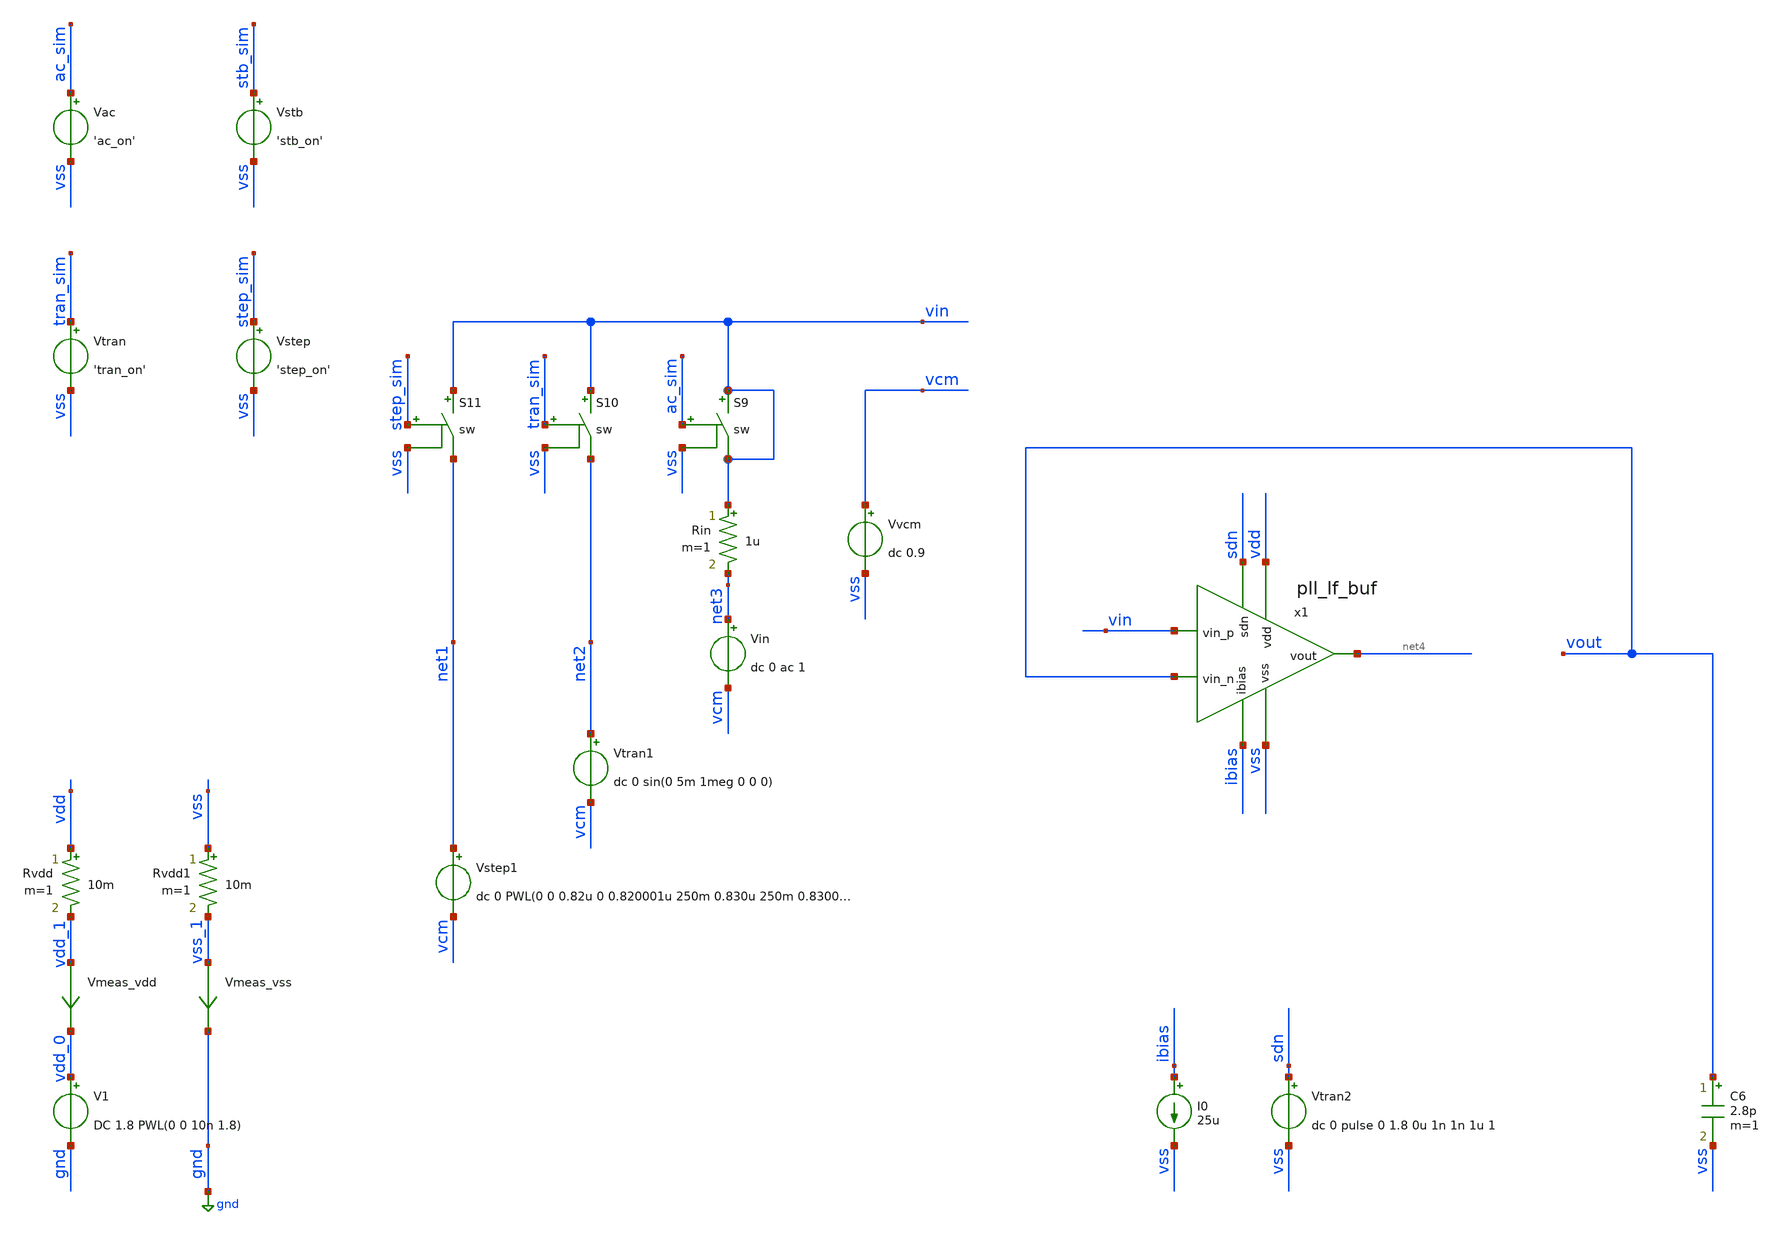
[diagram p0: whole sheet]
** sch_path: pll/pll_lf_buf/simulation/pll_lf_buf_tb.sch
**.subckt pll_lf_buf_tb
Vvcm vcm vss dc 0.9
C6 vout vss 2.8p m=1
Vtran tran_sim vss 'tran_on'
Vstep step_sim vss 'step_on'
Vstb stb_sim vss 'stb_on'
Vac ac_sim vss 'ac_on'
Vin net3 vcm dc 0 ac 1
S9 vin vin ac_sim vss sw
S10 vin net2 tran_sim vss sw
Vtran1 net2 vcm dc 0 sin(0 5m 1meg 0 0 0)
Vstep1 net1 vcm dc 0 PWL(0 0 0.82u 0 0.820001u 250m 0.830u 250m 0.830001u 0 0.86u 0 0.860001u -250m
+ 0.870u -250m 0.870001u 0)
S11 vin net1 step_sim vss sw
Rin vin net3 1u m=1
Vtran2 sdn vss dc 0 pulse 0 1.8 0u 1n 1n 1u 1
V1 vdd_0 gnd DC 1.8 PWL(0 0 10n 1.8)
Vmeas_vdd vdd_1 vdd_0 0
.save i(vmeas_vdd)
Vmeas_vss vss_1 gnd 0
.save i(vmeas_vss)
Rvdd vdd vdd_1 10m m=1
Rvdd1 vss vss_1 10m m=1
I0 ibias vss 25u
x1 vdd vin sdn vout net4 ibias vss pll_lf_buf
**** begin user architecture code


.param temp=27

.param ac_on=1
.param stb_on= 0
.param tran_on=0
.param step_on=0

.option savecurrents
.option rshunt = 1e12
*.option gmin = 1e-24
**.option method=Gear
**.option chgtol=1e-12


*.model switch1 aswitch(cntl_off=0.0 cntl_on=0.1 r_off=1e12 r_on=1.0 log=TRUE)
.model sw SW (ron=0.1 roff=1e12 vt=0.5 vh=0)

.control
* Main Amplifier
** Main Core OP params
save i(@m.x1.xm1.msky130_fd_pr__pfet_01v8[id])
save @m.x1.xm1.msky130_fd_pr__pfet_01v8[gm]
save v(@m.x1.xm1.msky130_fd_pr__pfet_01v8[vds])
save v(@m.x1.xm1.msky130_fd_pr__pfet_01v8[vgs])
save v(@m.x1.xm1.msky130_fd_pr__pfet_01v8[vth])
save v(@m.x1.xm1.msky130_fd_pr__pfet_01v8[vdsat])

save i(@m.x1.xm2.msky130_fd_pr__pfet_01v8[id])
save @m.x1.xm2.msky130_fd_pr__pfet_01v8[gm]
save v(@m.x1.xm2.msky130_fd_pr__pfet_01v8[vds])
save v(@m.x1.xm2.msky130_fd_pr__pfet_01v8[vgs])
save v(@m.x1.xm2.msky130_fd_pr__pfet_01v8[vth])
save v(@m.x1.xm2.msky130_fd_pr__pfet_01v8[vdsat])

save i(@m.x1.xm3.msky130_fd_pr__pfet_01v8[id])
save @m.x1.xm3.msky130_fd_pr__pfet_01v8[gm]
save v(@m.x1.xm3.msky130_fd_pr__pfet_01v8[vds])
save v(@m.x1.xm3.msky130_fd_pr__pfet_01v8[vgs])
save v(@m.x1.xm3.msky130_fd_pr__pfet_01v8[vth])
save v(@m.x1.xm3.msky130_fd_pr__pfet_01v8[vdsat])

save i(@m.x1.xm4.msky130_fd_pr__pfet_01v8[id])
save @m.x1.xm4.msky130_fd_pr__pfet_01v8[gm]
save v(@m.x1.xm4.msky130_fd_pr__pfet_01v8[vds])
save v(@m.x1.xm4.msky130_fd_pr__pfet_01v8[vgs])
save v(@m.x1.xm4.msky130_fd_pr__pfet_01v8[vth])
save v(@m.x1.xm4.msky130_fd_pr__pfet_01v8[vdsat])

save i(@m.x1.xm5.msky130_fd_pr__pfet_01v8[id])
save @m.x1.xm5.msky130_fd_pr__pfet_01v8[gm]
save v(@m.x1.xm5.msky130_fd_pr__pfet_01v8[vds])
save v(@m.x1.xm5.msky130_fd_pr__pfet_01v8[vgs])
save v(@m.x1.xm5.msky130_fd_pr__pfet_01v8[vth])
save v(@m.x1.xm5.msky130_fd_pr__pfet_01v8[vdsat])

save i(@m.x1.xm6.msky130_fd_pr__pfet_01v8[id])
save @m.x1.xm6.msky130_fd_pr__pfet_01v8[gm]
save v(@m.x1.xm6.msky130_fd_pr__pfet_01v8[vds])
save v(@m.x1.xm6.msky130_fd_pr__pfet_01v8[vgs])
save v(@m.x1.xm6.msky130_fd_pr__pfet_01v8[vth])
save v(@m.x1.xm6.msky130_fd_pr__pfet_01v8[vdsat])

save i(@m.x1.xm7.msky130_fd_pr__nfet_01v8[id])
save @m.x1.xm7.msky130_fd_pr__nfet_01v8[gm]
save v(@m.x1.xm7.msky130_fd_pr__nfet_01v8[vds])
save v(@m.x1.xm7.msky130_fd_pr__nfet_01v8[vgs])
save v(@m.x1.xm7.msky130_fd_pr__nfet_01v8[vth])
save v(@m.x1.xm7.msky130_fd_pr__nfet_01v8[vdsat])

save i(@m.x1.xm8.msky130_fd_pr__nfet_01v8[id])
save @m.x1.xm8.msky130_fd_pr__nfet_01v8[gm]
save v(@m.x1.xm8.msky130_fd_pr__nfet_01v8[vds])
save v(@m.x1.xm8.msky130_fd_pr__nfet_01v8[vgs])
save v(@m.x1.xm8.msky130_fd_pr__nfet_01v8[vth])
save v(@m.x1.xm8.msky130_fd_pr__nfet_01v8[vdsat])

save i(@m.x1.xm9.msky130_fd_pr__nfet_01v8[id])
save @m.x1.xm9.msky130_fd_pr__nfet_01v8[gm]
save v(@m.x1.xm9.msky130_fd_pr__nfet_01v8[vds])
save v(@m.x1.xm9.msky130_fd_pr__nfet_01v8[vgs])
save v(@m.x1.xm9.msky130_fd_pr__nfet_01v8[vth])
save v(@m.x1.xm9.msky130_fd_pr__nfet_01v8[vdsat])

save i(@m.x1.xm10.msky130_fd_pr__nfet_01v8[id])
save @m.x1.xm10.msky130_fd_pr__nfet_01v8[gm]
save v(@m.x1.xm10.msky130_fd_pr__nfet_01v8[vds])
save v(@m.x1.xm10.msky130_fd_pr__nfet_01v8[vgs])
save v(@m.x1.xm10.msky130_fd_pr__nfet_01v8[vth])
save v(@m.x1.xm10.msky130_fd_pr__nfet_01v8[vdsat])

save i(@m.x1.xm11.msky130_fd_pr__pfet_01v8[id])
save @m.x1.xm11.msky130_fd_pr__pfet_01v8[gm]
save v(@m.x1.xm11.msky130_fd_pr__pfet_01v8[vds])
save v(@m.x1.xm11.msky130_fd_pr__pfet_01v8[vgs])
save v(@m.x1.xm11.msky130_fd_pr__pfet_01v8[vth])
save v(@m.x1.xm11.msky130_fd_pr__pfet_01v8[vdsat])


** CMFB OP param
save i(@m.x1.xm28.msky130_fd_pr__pfet_01v8[id])
save @m.x1.xm28.msky130_fd_pr__pfet_01v8[gm]
save v(@m.x1.xm28.msky130_fd_pr__pfet_01v8[vds])
save v(@m.x1.xm28.msky130_fd_pr__pfet_01v8[vgs])
save v(@m.x1.xm28.msky130_fd_pr__pfet_01v8[vth])
save v(@m.x1.xm28.msky130_fd_pr__pfet_01v8[vdsat])

save i(@m.x1.xm29.msky130_fd_pr__pfet_01v8_lvt[id])
save @m.x1.xm29.msky130_fd_pr__pfet_01v8_lvt[gm]
save v(@m.x1.xm29.msky130_fd_pr__pfet_01v8_lvt[vds])
save v(@m.x1.xm29.msky130_fd_pr__pfet_01v8_lvt[vgs])
save v(@m.x1.xm29.msky130_fd_pr__pfet_01v8_lvt[vth])
save v(@m.x1.xm29.msky130_fd_pr__pfet_01v8_lvt[vdsat])

save i(@m.x1.xm30.msky130_fd_pr__pfet_01v8_lvt[id])
save @m.x1.xm30.msky130_fd_pr__pfet_01v8_lvt[gm]
save v(@m.x1.xm30.msky130_fd_pr__pfet_01v8_lvt[vds])
save v(@m.x1.xm30.msky130_fd_pr__pfet_01v8_lvt[vgs])
save v(@m.x1.xm30.msky130_fd_pr__pfet_01v8_lvt[vth])
save v(@m.x1.xm30.msky130_fd_pr__pfet_01v8_lvt[vdsat])

save i(@m.x1.xm31.msky130_fd_pr__pfet_01v8[id])
save @m.x1.xm31.msky130_fd_pr__pfet_01v8[gm]
save v(@m.x1.xm31.msky130_fd_pr__pfet_01v8[vds])
save v(@m.x1.xm31.msky130_fd_pr__pfet_01v8[vgs])
save v(@m.x1.xm31.msky130_fd_pr__pfet_01v8[vth])
save v(@m.x1.xm31.msky130_fd_pr__pfet_01v8[vdsat])

save i(@m.x1.xm32.msky130_fd_pr__pfet_01v8_lvt[id])
save @m.x1.xm32.msky130_fd_pr__pfet_01v8_lvt[gm]
save v(@m.x1.xm32.msky130_fd_pr__pfet_01v8_lvt[vds])
save v(@m.x1.xm32.msky130_fd_pr__pfet_01v8_lvt[vgs])
save v(@m.x1.xm32.msky130_fd_pr__pfet_01v8_lvt[vth])
save v(@m.x1.xm32.msky130_fd_pr__pfet_01v8_lvt[vdsat])

save i(@m.x1.xm33.msky130_fd_pr__pfet_01v8_lvt[id])
save @m.x1.xm33.msky130_fd_pr__pfet_01v8_lvt[gm]
save v(@m.x1.xm33.msky130_fd_pr__pfet_01v8_lvt[vds])
save v(@m.x1.xm33.msky130_fd_pr__pfet_01v8_lvt[vgs])
save v(@m.x1.xm33.msky130_fd_pr__pfet_01v8_lvt[vth])
save v(@m.x1.xm33.msky130_fd_pr__pfet_01v8_lvt[vdsat])

save i(@m.x1.xm34.msky130_fd_pr__nfet_01v8[id])
save @m.x1.xm34.msky130_fd_pr__nfet_01v8[gm]
save v(@m.x1.xm34.msky130_fd_pr__nfet_01v8[vds])
save v(@m.x1.xm34.msky130_fd_pr__nfet_01v8[vgs])
save v(@m.x1.xm34.msky130_fd_pr__nfet_01v8[vth])
save v(@m.x1.xm34.msky130_fd_pr__nfet_01v8[vdsat])

save i(@m.x1.xm35.msky130_fd_pr__nfet_01v8[id])
save @m.x1.xm35.msky130_fd_pr__nfet_01v8[gm]
save v(@m.x1.xm35.msky130_fd_pr__nfet_01v8[vds])
save v(@m.x1.xm35.msky130_fd_pr__nfet_01v8[vgs])
save v(@m.x1.xm35.msky130_fd_pr__nfet_01v8[vth])
save v(@m.x1.xm35.msky130_fd_pr__nfet_01v8[vdsat])

* Gain Booster Pside
** Main core OP parameters
save i(@m.x1.xgbp.xm1.msky130_fd_pr__nfet_01v8[id])
save @m.x1.xgbp.xm1.msky130_fd_pr__nfet_01v8[gm]
save v(@m.x1.xgbp.xm1.msky130_fd_pr__nfet_01v8[vds])
save v(@m.x1.xgbp.xm1.msky130_fd_pr__nfet_01v8[vgs])
save v(@m.x1.xgbp.xm1.msky130_fd_pr__nfet_01v8[vth])
save v(@m.x1.xgbp.xm1.msky130_fd_pr__nfet_01v8[vdsat])

save i(@m.x1.xgbp.xm2.msky130_fd_pr__nfet_01v8[id])
save @m.x1.xgbp.xm2.msky130_fd_pr__nfet_01v8[gm]
save v(@m.x1.xgbp.xm2.msky130_fd_pr__nfet_01v8[vds])
save v(@m.x1.xgbp.xm2.msky130_fd_pr__nfet_01v8[vgs])
save v(@m.x1.xgbp.xm2.msky130_fd_pr__nfet_01v8[vth])
save v(@m.x1.xgbp.xm2.msky130_fd_pr__nfet_01v8[vdsat])

save i(@m.x1.xgbp.xm3.msky130_fd_pr__nfet_01v8[id])
save @m.x1.xgbp.xm3.msky130_fd_pr__nfet_01v8[gm]
save v(@m.x1.xgbp.xm3.msky130_fd_pr__nfet_01v8[vds])
save v(@m.x1.xgbp.xm3.msky130_fd_pr__nfet_01v8[vgs])
save v(@m.x1.xgbp.xm3.msky130_fd_pr__nfet_01v8[vth])
save v(@m.x1.xgbp.xm3.msky130_fd_pr__nfet_01v8[vdsat])

save i(@m.x1.xgbp.xm4.msky130_fd_pr__pfet_01v8[id])
save @m.x1.xgbp.xm4.msky130_fd_pr__pfet_01v8[gm]
save v(@m.x1.xgbp.xm4.msky130_fd_pr__pfet_01v8[vds])
save v(@m.x1.xgbp.xm4.msky130_fd_pr__pfet_01v8[vgs])
save v(@m.x1.xgbp.xm4.msky130_fd_pr__pfet_01v8[vth])
save v(@m.x1.xgbp.xm4.msky130_fd_pr__pfet_01v8[vdsat])

save i(@m.x1.xgbp.xm5.msky130_fd_pr__pfet_01v8[id])
save @m.x1.xgbp.xm5.msky130_fd_pr__pfet_01v8[gm]
save v(@m.x1.xgbp.xm5.msky130_fd_pr__pfet_01v8[vds])
save v(@m.x1.xgbp.xm5.msky130_fd_pr__pfet_01v8[vgs])
save v(@m.x1.xgbp.xm5.msky130_fd_pr__pfet_01v8[vth])
save v(@m.x1.xgbp.xm5.msky130_fd_pr__pfet_01v8[vdsat])

save i(@m.x1.xgbp.xm6.msky130_fd_pr__pfet_01v8[id])
save @m.x1.xgbp.xm6.msky130_fd_pr__pfet_01v8[gm]
save v(@m.x1.xgbp.xm6.msky130_fd_pr__pfet_01v8[vds])
save v(@m.x1.xgbp.xm6.msky130_fd_pr__pfet_01v8[vgs])
save v(@m.x1.xgbp.xm6.msky130_fd_pr__pfet_01v8[vth])
save v(@m.x1.xgbp.xm6.msky130_fd_pr__pfet_01v8[vdsat])

save i(@m.x1.xgbp.xm7.msky130_fd_pr__pfet_01v8[id])
save @m.x1.xgbp.xm7.msky130_fd_pr__pfet_01v8[gm]
save v(@m.x1.xgbp.xm7.msky130_fd_pr__pfet_01v8[vds])
save v(@m.x1.xgbp.xm7.msky130_fd_pr__pfet_01v8[vgs])
save v(@m.x1.xgbp.xm7.msky130_fd_pr__pfet_01v8[vth])
save v(@m.x1.xgbp.xm7.msky130_fd_pr__pfet_01v8[vdsat])

save i(@m.x1.xgbp.xm8.msky130_fd_pr__nfet_01v8[id])
save @m.x1.xgbp.xm8.msky130_fd_pr__nfet_01v8[gm]
save v(@m.x1.xgbp.xm8.msky130_fd_pr__nfet_01v8[vds])
save v(@m.x1.xgbp.xm8.msky130_fd_pr__nfet_01v8[vgs])
save v(@m.x1.xgbp.xm8.msky130_fd_pr__nfet_01v8[vth])
save v(@m.x1.xgbp.xm8.msky130_fd_pr__nfet_01v8[vdsat])

save i(@m.x1.xgbp.xm9.msky130_fd_pr__nfet_01v8[id])
save @m.x1.xgbp.xm9.msky130_fd_pr__nfet_01v8[gm]
save v(@m.x1.xgbp.xm9.msky130_fd_pr__nfet_01v8[vds])
save v(@m.x1.xgbp.xm9.msky130_fd_pr__nfet_01v8[vgs])
save v(@m.x1.xgbp.xm9.msky130_fd_pr__nfet_01v8[vth])
save v(@m.x1.xgbp.xm9.msky130_fd_pr__nfet_01v8[vdsat])

save i(@m.x1.xgbp.xm10.msky130_fd_pr__nfet_01v8[id])
save @m.x1.xgbp.xm10.msky130_fd_pr__nfet_01v8[gm]
save v(@m.x1.xgbp.xm10.msky130_fd_pr__nfet_01v8[vds])
save v(@m.x1.xgbp.xm10.msky130_fd_pr__nfet_01v8[vgs])
save v(@m.x1.xgbp.xm10.msky130_fd_pr__nfet_01v8[vth])
save v(@m.x1.xgbp.xm10.msky130_fd_pr__nfet_01v8[vdsat])

save i(@m.x1.xgbp.xm11.msky130_fd_pr__nfet_01v8[id])
save @m.x1.xgbp.xm11.msky130_fd_pr__nfet_01v8[gm]
save v(@m.x1.xgbp.xm11.msky130_fd_pr__nfet_01v8[vds])
save v(@m.x1.xgbp.xm11.msky130_fd_pr__nfet_01v8[vgs])
save v(@m.x1.xgbp.xm11.msky130_fd_pr__nfet_01v8[vth])
save v(@m.x1.xgbp.xm11.msky130_fd_pr__nfet_01v8[vdsat])


** CMFB OP param
save i(@m.x1.xgbp.xm28.msky130_fd_pr__pfet_01v8[id])
save @m.x1.xgbp.xm28.msky130_fd_pr__pfet_01v8[gm]
save v(@m.x1.xgbp.xm28.msky130_fd_pr__pfet_01v8[vds])
save v(@m.x1.xgbp.xm28.msky130_fd_pr__pfet_01v8[vgs])
save v(@m.x1.xgbp.xm28.msky130_fd_pr__pfet_01v8[vth])
save v(@m.x1.xgbp.xm28.msky130_fd_pr__pfet_01v8[vdsat])

save i(@m.x1.xgbp.xm29.msky130_fd_pr__pfet_01v8_lvt[id])
save @m.x1.xgbp.xm29.msky130_fd_pr__pfet_01v8_lvt[gm]
save v(@m.x1.xgbp.xm29.msky130_fd_pr__pfet_01v8_lvt[vds])
save v(@m.x1.xgbp.xm29.msky130_fd_pr__pfet_01v8_lvt[vgs])
save v(@m.x1.xgbp.xm29.msky130_fd_pr__pfet_01v8_lvt[vth])
save v(@m.x1.xgbp.xm29.msky130_fd_pr__pfet_01v8_lvt[vdsat])

save i(@m.x1.xgbp.xm30.msky130_fd_pr__pfet_01v8_lvt[id])
save @m.x1.xgbp.xm30.msky130_fd_pr__pfet_01v8_lvt[gm]
save v(@m.x1.xgbp.xm30.msky130_fd_pr__pfet_01v8_lvt[vds])
save v(@m.x1.xgbp.xm30.msky130_fd_pr__pfet_01v8_lvt[vgs])
save v(@m.x1.xgbp.xm30.msky130_fd_pr__pfet_01v8_lvt[vth])
save v(@m.x1.xgbp.xm30.msky130_fd_pr__pfet_01v8_lvt[vdsat])

save i(@m.x1.xgbp.xm31.msky130_fd_pr__pfet_01v8[id])
save @m.x1.xgbp.xm31.msky130_fd_pr__pfet_01v8[gm]
save v(@m.x1.xgbp.xm31.msky130_fd_pr__pfet_01v8[vds])
save v(@m.x1.xgbp.xm31.msky130_fd_pr__pfet_01v8[vgs])
save v(@m.x1.xgbp.xm31.msky130_fd_pr__pfet_01v8[vth])
save v(@m.x1.xgbp.xm31.msky130_fd_pr__pfet_01v8[vdsat])

save i(@m.x1.xgbp.xm32.msky130_fd_pr__pfet_01v8_lvt[id])
save @m.x1.xgbp.xm32.msky130_fd_pr__pfet_01v8_lvt[gm]
save v(@m.x1.xgbp.xm32.msky130_fd_pr__pfet_01v8_lvt[vds])
save v(@m.x1.xgbp.xm32.msky130_fd_pr__pfet_01v8_lvt[vgs])
save v(@m.x1.xgbp.xm32.msky130_fd_pr__pfet_01v8_lvt[vth])
save v(@m.x1.xgbp.xm32.msky130_fd_pr__pfet_01v8_lvt[vdsat])

save i(@m.x1.xgbp.xm33.msky130_fd_pr__pfet_01v8_lvt[id])
save @m.x1.xgbp.xm33.msky130_fd_pr__pfet_01v8_lvt[gm]
save v(@m.x1.xgbp.xm33.msky130_fd_pr__pfet_01v8_lvt[vds])
save v(@m.x1.xgbp.xm33.msky130_fd_pr__pfet_01v8_lvt[vgs])
save v(@m.x1.xgbp.xm33.msky130_fd_pr__pfet_01v8_lvt[vth])
save v(@m.x1.xgbp.xm33.msky130_fd_pr__pfet_01v8_lvt[vdsat])

save i(@m.x1.xgbp.xm34.msky130_fd_pr__nfet_01v8[id])
save @m.x1.xgbp.xm34.msky130_fd_pr__nfet_01v8[gm]
save v(@m.x1.xgbp.xm34.msky130_fd_pr__nfet_01v8[vds])
save v(@m.x1.xgbp.xm34.msky130_fd_pr__nfet_01v8[vgs])
save v(@m.x1.xgbp.xm34.msky130_fd_pr__nfet_01v8[vth])
save v(@m.x1.xgbp.xm34.msky130_fd_pr__nfet_01v8[vdsat])

save i(@m.x1.xgbp.xm35.msky130_fd_pr__nfet_01v8[id])
save @m.x1.xgbp.xm35.msky130_fd_pr__nfet_01v8[gm]
save v(@m.x1.xgbp.xm35.msky130_fd_pr__nfet_01v8[vds])
save v(@m.x1.xgbp.xm35.msky130_fd_pr__nfet_01v8[vgs])
save v(@m.x1.xgbp.xm35.msky130_fd_pr__nfet_01v8[vth])
save v(@m.x1.xgbp.xm35.msky130_fd_pr__nfet_01v8[vdsat])


* #################################################################
* #
* #                         OPERATING POINT
* #
* #################################################################
save all
save v(vin)
save v(vout)

op
set filetype=binary
write pll_lf_buf_tb.raw all


* #################################################################
* #
* #                          AC SIMULATION
* #
* #################################################################
alterparam ac_on=1
alterparam stb_on=0
alterparam tran_on=0
alterparam step_on=0
reset
save all
save v(vin)
save v(vout)

ac dec 100 1 1T
set filetype=ascii
write  pll_lf_buf_tb_ac.raw all

plot dB(v(vout)/v(vin))


* #################################################################
* #
* #                     STABILITY SIMULATION
* #
* #################################################################
alterparam ac_on=1
alterparam stb_on=0
alterparam tran_on=0
alterparam step_on=0
reset
save all
save v(vin)
save v(vout)

*set mag_ac = @Vin[acmag]
alter @Vin[acmag]=0
*set imp_ac = @Rin[r]
alter @Rin[r]=1e12

alter @v.xstbprb.Vprobe1[acmag]=1
alter @i.xstbprb.Iprobe1[acmag]=0
ac dec 100 1 1T
set filetype=ascii
write pll_lf_buf_tb_ol_0.raw all

alter @v.xstbprb.Vprobe1[acmag]=0
alter @i.xstbprb.Iprobe1[acmag]=1
ac dec 100 1 1T
set filetype=ascii
write pll_lf_buf_tb_ol_1.raw all

alter @v.xstbprb.Vprobe1[acmag]=0
alter @i.xstbprb.Iprobe1[acmag]=0

*alter @Vin[acmag]=mag_ac
*alter @Rin[r]=imp_ac
alter @Vin[acmag]=1
alter @Rin[r]=1u


* EXTRACT REQUIRED DATA
let ip11 = ac2.i(v.xstbprb.Vprobe1)
let ip12 = ac2.i(v.xstbprb.Vprobe2)
let ip21 = ac3.i(v.xstbprb.Vprobe1)
let ip22 = ac3.i(v.xstbprb.Vprobe2)
let vprb1 = ac2.xstbprb.probe_p
let vprb2 = ac3.xstbprb.probe_p
*let vprb1 = ac2.xstbprb.probe_p-ac2.xstbprb.probe_n
*let vprb2 = ac3.xstbprb.probe_p-ac3.xstbprb.probe_n


* MIDDLEBROOK
let loopgain_middlebrook = 1/(vprb1+ip22)-1
let phase_middlebrook = 180/PI*vp(loopgain_middlebrook)

* TIAN
let loopgain_tian = 1/(1/(2*(ip11*vprb2-vprb1*ip21)+vprb1+ip21)-1)
let phase_tian = 180/PI*vp(loopgain_tian)

* CALCULATE & PLOT
plot vdb(loopgain_tian)
plot phase_tian

plot vdb(loopgain_middlebrook)
plot phase_middlebrook

plot vdb(loopgain_middlebrook) vdb(loopgain_tian)
plot phase_middlebrook phase_tian

* MEASUREMENT
echo --
echo --
let pm_deg=0
let pm_freq=0
meas ac pm_deg find phase_tian when vdb(loopgain_tian)=0
meas ac pm_freq find frequency when vdb(loopgain_tian)=0

let gm_db=0
let gm_freq=0
meas ac gm_db find vdb(loopgain_tian) when vp(loopgain_tian)=0
meas ac gm_freq find frequency when vp(loopgain_tian)=0

*meas ac 3db_f when phase_tian=135
*meas ac 0db_f when vdb(loopgain_tian)=0
*meas ac dc_gain find vdb(loopgain_tian) at=0.01
*meas ac m6dB when vdB(loopgain_tian)=-6
echo --
echo --

* SAVE DATA
set filetype=ascii
write  pll_lf_buf_tb_ol.raw loopgain_middlebrook loopgain_tian pm_deg pm_freq gm_db gm_freq

* #################################################################
* #
* #                       NOISE SIMULATION
* #
* #################################################################
alterparam ac_on=1
alterparam stb_on=0
alterparam tran_on=0
alterparam step_on=0
reset
save all
save v(vin)
save v(vout)

set sqrnoise
noise v(vout) vin dec 100 1 1T
set filetype=ascii
write  pll_lf_buf_se_tb_noise.raw all noise3.inoise_spectrum noise3.onoise_spectrum

plot noise3.inoise_spectrum noise3.onoise_spectrum
print inoise_total
print onoise_total

* #################################################################
* #
* #                 TRANSIENT SINE WAVE REGIME
* #
* #################################################################
alterparam ac_on=0
alterparam stb_on=0
alterparam tran_on=1
alterparam step_on=0
reset
save all
save v(vin)
save v(vout)

set imp_ac = @Rin[r]
alter @Rin[r]=1e12

tran 0.1n 10u uic
set filetype=ascii
write pll_lf_buf_tb_tran.raw all

alter @Rin[r]=imp_ac

plot v(vin) v(vout)


* #################################################################
* #
* #                   TRANSIENT STEP RESPONSE
* #
* #################################################################
*alterparam ac_on = 0
*alterparam stb_on = 0
*alterparam tran_on = 0
*alterparam step_on = 1
*reset
*save all
*save v(vin)
*save v(vout)
*
*set imp_ac = @Rin[r]
*alter @Rin[r]=1e12
*
*tran 0.1n 0.9u 0.8u
*set filetype=ascii
*write pll_lf_buf_tb_step.raw all
*
*alter @Rin[r]=imp_ac
*
*plot v(vin) v(vout)

.endc



.options wnflag=1
.include $::SKYWATER_MODELS/cells/nfet_01v8/sky130_fd_pr__nfet_01v8__tt.corner.spice
.include $::SKYWATER_MODELS/cells/nfet_01v8_lvt/sky130_fd_pr__nfet_01v8_lvt__tt.corner.spice
.include $::SKYWATER_MODELS/cells/pfet_01v8/sky130_fd_pr__pfet_01v8__tt.corner.spice
.include $::SKYWATER_MODELS/cells/nfet_03v3_nvt/sky130_fd_pr__nfet_03v3_nvt__tt.corner.spice
.include $::SKYWATER_MODELS/cells/nfet_05v0_nvt/sky130_fd_pr__nfet_05v0_nvt__tt.corner.spice
.include $::SKYWATER_MODELS/cells/esd_nfet_01v8/sky130_fd_pr__esd_nfet_01v8__tt.corner.spice
.include $::SKYWATER_MODELS/cells/pfet_01v8_lvt/sky130_fd_pr__pfet_01v8_lvt__tt.corner.spice
.include $::SKYWATER_MODELS/cells/pfet_01v8_hvt/sky130_fd_pr__pfet_01v8_hvt__tt.corner.spice
.include $::SKYWATER_MODELS/cells/esd_pfet_g5v0d10v5/sky130_fd_pr__esd_pfet_g5v0d10v5__tt.corner.spice
.include $::SKYWATER_MODELS/cells/pfet_g5v0d10v5/sky130_fd_pr__pfet_g5v0d10v5__tt.corner.spice
.include $::SKYWATER_MODELS/cells/pfet_g5v0d16v0/sky130_fd_pr__pfet_g5v0d16v0__tt.corner.spice
.include $::SKYWATER_MODELS/cells/nfet_g5v0d10v5/sky130_fd_pr__nfet_g5v0d10v5__tt.corner.spice
.include $::SKYWATER_MODELS/cells/nfet_g5v0d16v0/sky130_fd_pr__nfet_g5v0d16v0__tt_discrete.corner.spice
.include $::SKYWATER_MODELS/cells/esd_nfet_g5v0d10v5/sky130_fd_pr__esd_nfet_g5v0d10v5__tt.corner.spice
.include $::SKYWATER_MODELS/models/corners/tt/nonfet.spice
* Mismatch parameters
.include $::SKYWATER_MODELS/cells/nfet_01v8/sky130_fd_pr__nfet_01v8__mismatch.corner.spice
.include $::SKYWATER_MODELS/cells/pfet_01v8/sky130_fd_pr__pfet_01v8__mismatch.corner.spice
.include $::SKYWATER_MODELS/cells/nfet_01v8_lvt/sky130_fd_pr__nfet_01v8_lvt__mismatch.corner.spice
.include $::SKYWATER_MODELS/cells/pfet_01v8_lvt/sky130_fd_pr__pfet_01v8_lvt__mismatch.corner.spice
.include $::SKYWATER_MODELS/cells/pfet_01v8_hvt/sky130_fd_pr__pfet_01v8_hvt__mismatch.corner.spice
.include $::SKYWATER_MODELS/cells/nfet_g5v0d10v5/sky130_fd_pr__nfet_g5v0d10v5__mismatch.corner.spice
.include $::SKYWATER_MODELS/cells/pfet_g5v0d10v5/sky130_fd_pr__pfet_g5v0d10v5__mismatch.corner.spice
.include $::SKYWATER_MODELS/cells/nfet_05v0_nvt/sky130_fd_pr__nfet_05v0_nvt__mismatch.corner.spice
.include $::SKYWATER_MODELS/cells/nfet_03v3_nvt/sky130_fd_pr__nfet_03v3_nvt__mismatch.corner.spice
* Resistor$::SKYWATER_MODELS/Capacitor
.include $::SKYWATER_MODELS/models/r+c/res_typical__cap_typical.spice
.include $::SKYWATER_MODELS/models/r+c/res_typical__cap_typical__lin.spice
* Special cells
.include $::SKYWATER_MODELS/models/corners/tt/specialized_cells.spice
* All models
.include $::SKYWATER_MODELS/models/all.spice
* Corner
.include $::SKYWATER_MODELS/models/corners/tt/rf.spice

**** end user architecture code
**.ends

* expanding   symbol:  test_jens/pll/pll_lf_buf/pll_lf_buf.sym # of pins=7
** sym_path: pll/pll_lf_buf/xschem/pll_lf_buf.sym
** sch_path: pll/pll_lf_buf/xschem/pll_lf_buf.sch
.subckt pll_lf_buf vdd vin_p sdn vin_n vout ibias vss
*.iopin vss
*.iopin vdd
*.ipin vin_p
*.ipin vin_n
*.iopin ibias
*.opin vout
*.ipin sdn
XM1 net4 vin_p net1 vdd sky130_fd_pr__pfet_01v8 L=0.15 W=16 nf=2 ad='int((nf+1)/2) * W/nf * 0.29' as='int((nf+2)/2) * W/nf * 0.29'
+ pd='2*int((nf+1)/2) * (W/nf + 0.29)' ps='2*int((nf+2)/2) * (W/nf + 0.29)' nrd='0.29 / W' nrs='0.29 / W'
+ sa=0 sb=0 sd=0 mult=8 m=8
XM2 net5 vin_n net1 vdd sky130_fd_pr__pfet_01v8 L=0.15 W=16 nf=2 ad='int((nf+1)/2) * W/nf * 0.29' as='int((nf+2)/2) * W/nf * 0.29'
+ pd='2*int((nf+1)/2) * (W/nf + 0.29)' ps='2*int((nf+2)/2) * (W/nf + 0.29)' nrd='0.29 / W' nrs='0.29 / W'
+ sa=0 sb=0 sd=0 mult=8 m=8
XM3 vbn vbp_casc net2 vdd sky130_fd_pr__pfet_01v8 L=0.3 W=16 nf=2 ad='int((nf+1)/2) * W/nf * 0.29' as='int((nf+2)/2) * W/nf * 0.29'
+ pd='2*int((nf+1)/2) * (W/nf + 0.29)' ps='2*int((nf+2)/2) * (W/nf + 0.29)' nrd='0.29 / W' nrs='0.29 / W'
+ sa=0 sb=0 sd=0 mult=8 m=8
XM4 vout vbp_casc net3 vdd sky130_fd_pr__pfet_01v8 L=0.3 W=16 nf=2 ad='int((nf+1)/2) * W/nf * 0.29' as='int((nf+2)/2) * W/nf * 0.29'
+ pd='2*int((nf+1)/2) * (W/nf + 0.29)' ps='2*int((nf+2)/2) * (W/nf + 0.29)' nrd='0.29 / W' nrs='0.29 / W'
+ sa=0 sb=0 sd=0 mult=8 m=8
XM5 net2 vbp vdd vdd sky130_fd_pr__pfet_01v8 L=0.3 W=16 nf=2 ad='int((nf+1)/2) * W/nf * 0.29' as='int((nf+2)/2) * W/nf * 0.29'
+ pd='2*int((nf+1)/2) * (W/nf + 0.29)' ps='2*int((nf+2)/2) * (W/nf + 0.29)' nrd='0.29 / W' nrs='0.29 / W'
+ sa=0 sb=0 sd=0 mult=8 m=8
XM6 net3 vbp vdd vdd sky130_fd_pr__pfet_01v8 L=0.3 W=16 nf=2 ad='int((nf+1)/2) * W/nf * 0.29' as='int((nf+2)/2) * W/nf * 0.29'
+ pd='2*int((nf+1)/2) * (W/nf + 0.29)' ps='2*int((nf+2)/2) * (W/nf + 0.29)' nrd='0.29 / W' nrs='0.29 / W'
+ sa=0 sb=0 sd=0 mult=8 m=8
XM7 vbn vbn_casc net4 vss sky130_fd_pr__nfet_01v8 L=0.3 W=8 nf=2 ad='int((nf+1)/2) * W/nf * 0.29' as='int((nf+2)/2) * W/nf * 0.29'
+ pd='2*int((nf+1)/2) * (W/nf + 0.29)' ps='2*int((nf+2)/2) * (W/nf + 0.29)' nrd='0.29 / W' nrs='0.29 / W'
+ sa=0 sb=0 sd=0 mult=8 m=8
XM8 vout vbn_casc net5 vss sky130_fd_pr__nfet_01v8 L=0.3 W=8 nf=2 ad='int((nf+1)/2) * W/nf * 0.29' as='int((nf+2)/2) * W/nf * 0.29'
+ pd='2*int((nf+1)/2) * (W/nf + 0.29)' ps='2*int((nf+2)/2) * (W/nf + 0.29)' nrd='0.29 / W' nrs='0.29 / W'
+ sa=0 sb=0 sd=0 mult=8 m=8
XM9 net4 vbn vss vss sky130_fd_pr__nfet_01v8 L=0.3 W=8 nf=2 ad='int((nf+1)/2) * W/nf * 0.29' as='int((nf+2)/2) * W/nf * 0.29'
+ pd='2*int((nf+1)/2) * (W/nf + 0.29)' ps='2*int((nf+2)/2) * (W/nf + 0.29)' nrd='0.29 / W' nrs='0.29 / W'
+ sa=0 sb=0 sd=0 mult=8 m=8
XM10 net5 vbn vss vss sky130_fd_pr__nfet_01v8 L=0.3 W=8 nf=2 ad='int((nf+1)/2) * W/nf * 0.29' as='int((nf+2)/2) * W/nf * 0.29'
+ pd='2*int((nf+1)/2) * (W/nf + 0.29)' ps='2*int((nf+2)/2) * (W/nf + 0.29)' nrd='0.29 / W' nrs='0.29 / W'
+ sa=0 sb=0 sd=0 mult=8 m=8
XM11 net1 vbp vdd vdd sky130_fd_pr__pfet_01v8 L=0.3 W=8 nf=2 ad='int((nf+1)/2) * W/nf * 0.29' as='int((nf+2)/2) * W/nf * 0.29'
+ pd='2*int((nf+1)/2) * (W/nf + 0.29)' ps='2*int((nf+2)/2) * (W/nf + 0.29)' nrd='0.29 / W' nrs='0.29 / W'
+ sa=0 sb=0 sd=0 mult=8 m=8
XM12 net9 net10 vdd vdd sky130_fd_pr__pfet_01v8 L=0.3 W=16 nf=2 ad='int((nf+1)/2) * W/nf * 0.29' as='int((nf+2)/2) * W/nf * 0.29'
+ pd='2*int((nf+1)/2) * (W/nf + 0.29)' ps='2*int((nf+2)/2) * (W/nf + 0.29)' nrd='0.29 / W' nrs='0.29 / W'
+ sa=0 sb=0 sd=0 mult=1 m=1
XM13 net6 vbp vdd vdd sky130_fd_pr__pfet_01v8 L=0.3 W=16 nf=2 ad='int((nf+1)/2) * W/nf * 0.29' as='int((nf+2)/2) * W/nf * 0.29'
+ pd='2*int((nf+1)/2) * (W/nf + 0.29)' ps='2*int((nf+2)/2) * (W/nf + 0.29)' nrd='0.29 / W' nrs='0.29 / W'
+ sa=0 sb=0 sd=0 mult=1 m=1
XM14 net10 net8 net9 vdd sky130_fd_pr__pfet_01v8 L=0.3 W=16 nf=2 ad='int((nf+1)/2) * W/nf * 0.29' as='int((nf+2)/2) * W/nf * 0.29'
+ pd='2*int((nf+1)/2) * (W/nf + 0.29)' ps='2*int((nf+2)/2) * (W/nf + 0.29)' nrd='0.29 / W' nrs='0.29 / W'
+ sa=0 sb=0 sd=0 mult=1 m=1
XM15 vbn_casc vbp_casc net6 vdd sky130_fd_pr__pfet_01v8 L=0.3 W=16 nf=2 ad='int((nf+1)/2) * W/nf * 0.29'
+ as='int((nf+2)/2) * W/nf * 0.29' pd='2*int((nf+1)/2) * (W/nf + 0.29)' ps='2*int((nf+2)/2) * (W/nf + 0.29)'
+ nrd='0.29 / W' nrs='0.29 / W' sa=0 sb=0 sd=0 mult=1 m=1
XM16 vbn_casc vbn_casc vss vss sky130_fd_pr__nfet_01v8 L=1.2 W=4 nf=2 ad='int((nf+1)/2) * W/nf * 0.29'
+ as='int((nf+2)/2) * W/nf * 0.29' pd='2*int((nf+1)/2) * (W/nf + 0.29)' ps='2*int((nf+2)/2) * (W/nf + 0.29)'
+ nrd='0.29 / W' nrs='0.29 / W' sa=0 sb=0 sd=0 mult=1 m=1
XM17 net7 vbn_casc vss vss sky130_fd_pr__nfet_01v8 L=1.2 W=4 nf=2 ad='int((nf+1)/2) * W/nf * 0.29' as='int((nf+2)/2) * W/nf * 0.29'
+ pd='2*int((nf+1)/2) * (W/nf + 0.29)' ps='2*int((nf+2)/2) * (W/nf + 0.29)' nrd='0.29 / W' nrs='0.29 / W'
+ sa=0 sb=0 sd=0 mult=1 m=1
XM18 net7 net7 vdd vdd sky130_fd_pr__pfet_01v8 L=1.2 W=16 nf=2 ad='int((nf+1)/2) * W/nf * 0.29' as='int((nf+2)/2) * W/nf * 0.29'
+ pd='2*int((nf+1)/2) * (W/nf + 0.29)' ps='2*int((nf+2)/2) * (W/nf + 0.29)' nrd='0.29 / W' nrs='0.29 / W'
+ sa=0 sb=0 sd=0 mult=1 m=1
XM19 vbn sdn vss vss sky130_fd_pr__nfet_01v8 L=0.3 W=1 nf=1 ad='int((nf+1)/2) * W/nf * 0.29' as='int((nf+2)/2) * W/nf * 0.29'
+ pd='2*int((nf+1)/2) * (W/nf + 0.29)' ps='2*int((nf+2)/2) * (W/nf + 0.29)' nrd='0.29 / W' nrs='0.29 / W'
+ sa=0 sb=0 sd=0 mult=1 m=1
XM20 vbn_casc sdn vss vss sky130_fd_pr__nfet_01v8 L=0.3 W=1 nf=1 ad='int((nf+1)/2) * W/nf * 0.29' as='int((nf+2)/2) * W/nf * 0.29'
+ pd='2*int((nf+1)/2) * (W/nf + 0.29)' ps='2*int((nf+2)/2) * (W/nf + 0.29)' nrd='0.29 / W' nrs='0.29 / W'
+ sa=0 sb=0 sd=0 mult=1 m=1
XM21 vbp sdn_b vdd vdd sky130_fd_pr__pfet_01v8 L=0.3 W=1 nf=1 ad='int((nf+1)/2) * W/nf * 0.29' as='int((nf+2)/2) * W/nf * 0.29'
+ pd='2*int((nf+1)/2) * (W/nf + 0.29)' ps='2*int((nf+2)/2) * (W/nf + 0.29)' nrd='0.29 / W' nrs='0.29 / W'
+ sa=0 sb=0 sd=0 mult=1 m=1
XM22 vbp_casc sdn_b vdd vdd sky130_fd_pr__pfet_01v8 L=0.3 W=1 nf=1 ad='int((nf+1)/2) * W/nf * 0.29' as='int((nf+2)/2) * W/nf * 0.29'
+ pd='2*int((nf+1)/2) * (W/nf + 0.29)' ps='2*int((nf+2)/2) * (W/nf + 0.29)' nrd='0.29 / W' nrs='0.29 / W'
+ sa=0 sb=0 sd=0 mult=1 m=1
XM23 net8 sdn_b ibias vss sky130_fd_pr__nfet_01v8 L=0.15 W=4 nf=8 ad='int((nf+1)/2) * W/nf * 0.29' as='int((nf+2)/2) * W/nf * 0.29'
+ pd='2*int((nf+1)/2) * (W/nf + 0.29)' ps='2*int((nf+2)/2) * (W/nf + 0.29)' nrd='0.29 / W' nrs='0.29 / W'
+ sa=0 sb=0 sd=0 mult=1 m=1
**** begin user architecture code

.include $::SKYWATER_STDCELLS/cells/inv/sky130_fd_sc_hd__inv_1.spice
.include $::SKYWATER_STDCELLS/cells/inv/sky130_fd_sc_hd__inv_2.spice
.include $::SKYWATER_STDCELLS/cells/inv/sky130_fd_sc_hd__inv_4.spice
.include $::SKYWATER_STDCELLS/cells/inv/sky130_fd_sc_hd__inv_8.spice

**** end user architecture code
x1 sdn vss vss vdd vdd sdn_b sky130_fd_sc_hd__inv_1
R1 net10 net8 8k m=1
R2 vbp_casc net8 1 m=1
R3 vbp net10 1 m=1
XM24 ibias sdn net8 vdd sky130_fd_pr__pfet_01v8 L=0.15 W=12 nf=8 ad='int((nf+1)/2) * W/nf * 0.29' as='int((nf+2)/2) * W/nf * 0.29'
+ pd='2*int((nf+1)/2) * (W/nf + 0.29)' ps='2*int((nf+2)/2) * (W/nf + 0.29)' nrd='0.29 / W' nrs='0.29 / W'
+ sa=0 sb=0 sd=0 mult=1 m=1
.ends

.GLOBAL gnd
.end
